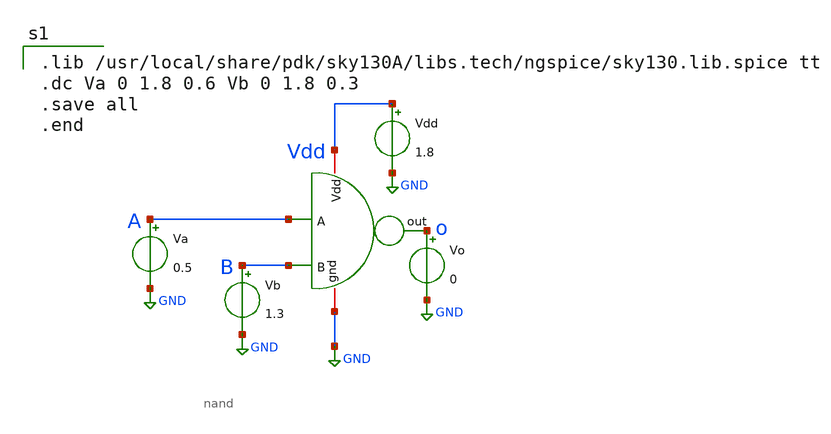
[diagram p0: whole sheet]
** sch_path: Gates/NAND/Schematic/nand_tb.sch
**.subckt nand_tb
x1 Vdd o B GND A nand
Va A GND 0.5
Vb B GND 1.3
Vdd Vdd GND 1.8
Vo o GND 0
**** begin user architecture code

.lib /usr/local/share/pdk/sky130A/libs.tech/ngspice/sky130.lib.spice tt
.dc Va 0 1.8 0.6 Vb 0 1.8 0.3
.save all
.end

**** end user architecture code
**.ends

* expanding   symbol:  nand.sym # of pins=5
** sym_path: Gates/NAND/Schematic/nand.sym
** sch_path: Gates/NAND/Schematic/nand.sch
.subckt nand Vdd out B gnd A
*.opin out
*.iopin Vdd
*.iopin gnd
*.ipin A
*.ipin B
XM1 out A net1 gnd sky130_fd_pr__nfet_01v8 L=0.15 W=1 nf=1 ad='int((nf+1)/2) * W/nf * 0.29' as='int((nf+2)/2) * W/nf * 0.29'
+ pd='2*int((nf+1)/2) * (W/nf + 0.29)' ps='2*int((nf+2)/2) * (W/nf + 0.29)' nrd='0.29 / W' nrs='0.29 / W'
+ sa=0 sb=0 sd=0 mult=1 m=1
XM2 out A Vdd Vdd sky130_fd_pr__pfet_01v8 L=0.15 W=2 nf=1 ad='int((nf+1)/2) * W/nf * 0.29' as='int((nf+2)/2) * W/nf * 0.29'
+ pd='2*int((nf+1)/2) * (W/nf + 0.29)' ps='2*int((nf+2)/2) * (W/nf + 0.29)' nrd='0.29 / W' nrs='0.29 / W'
+ sa=0 sb=0 sd=0 mult=1 m=1
XM3 out B Vdd Vdd sky130_fd_pr__pfet_01v8 L=0.15 W=2 nf=1 ad='int((nf+1)/2) * W/nf * 0.29' as='int((nf+2)/2) * W/nf * 0.29'
+ pd='2*int((nf+1)/2) * (W/nf + 0.29)' ps='2*int((nf+2)/2) * (W/nf + 0.29)' nrd='0.29 / W' nrs='0.29 / W'
+ sa=0 sb=0 sd=0 mult=1 m=1
XM4 net1 B gnd gnd sky130_fd_pr__nfet_01v8 L=0.15 W=1 nf=1 ad='int((nf+1)/2) * W/nf * 0.29' as='int((nf+2)/2) * W/nf * 0.29'
+ pd='2*int((nf+1)/2) * (W/nf + 0.29)' ps='2*int((nf+2)/2) * (W/nf + 0.29)' nrd='0.29 / W' nrs='0.29 / W'
+ sa=0 sb=0 sd=0 mult=1 m=1
.ends

.GLOBAL GND
.end
